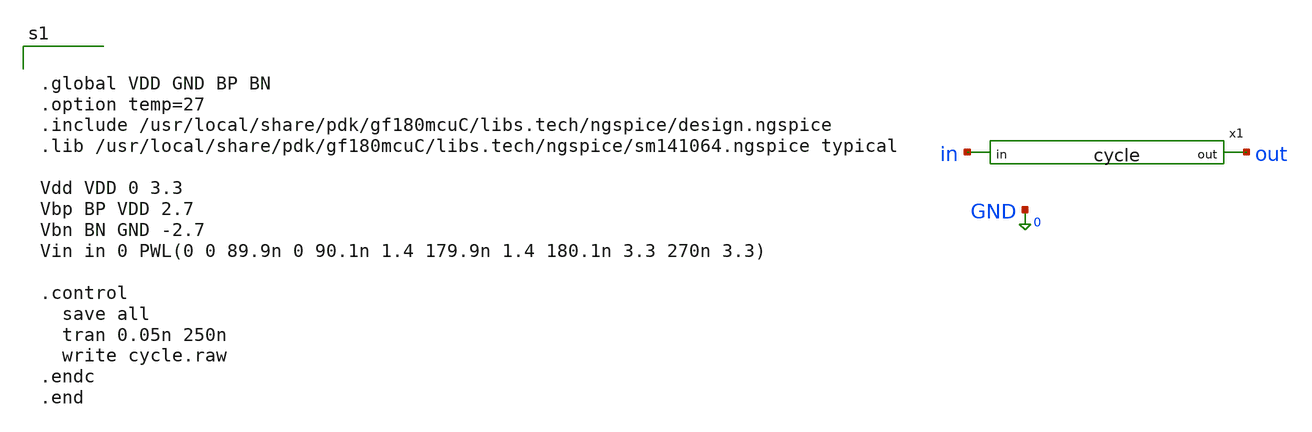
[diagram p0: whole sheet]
** sch_path: xschem_designs/cycle_TB.sch
**.subckt cycle_TB
x1 out in cycle
**** begin user architecture code


.global VDD GND BP BN
.option temp=27
.include /usr/local/share/pdk/gf180mcuC/libs.tech/ngspice/design.ngspice
.lib /usr/local/share/pdk/gf180mcuC/libs.tech/ngspice/sm141064.ngspice typical

Vdd VDD 0 3.3
Vbp BP VDD 2.7
Vbn BN GND -2.7
Vin in 0 PWL(0 0 89.9n 0 90.1n 1.4 179.9n 1.4 180.1n 3.3 270n 3.3)

.control
  save all
  tran 0.05n 250n
  write cycle.raw
.endc
.end


**** end user architecture code
**.ends

* expanding   symbol:  xschem_designs/cycle.sym # of pins=2
** sym_path: xschem_designs/cycle.sym
** sch_path: xschem_designs/cycle.sch
.subckt cycle out in
*.ipin in
*.opin out
XM225 out out net2 GND nfet_03v3 L=2.24u W=0.22u nf=1 ad='int((nf+1)/2) * W/nf * 0.18u' as='int((nf+2)/2) * W/nf * 0.18u'
+ pd='2*int((nf+1)/2) * (W/nf + 0.18u)' ps='2*int((nf+2)/2) * (W/nf + 0.18u)' nrd='0.18u / W' nrs='0.18u / W'
+ sa=0 sb=0 sd=0 m=1 par=1
XM226 out out net3 VDD pfet_03v3 L=1.12u W=0.22u nf=1 ad='int((nf+1)/2) * W/nf * 0.18u' as='int((nf+2)/2) * W/nf * 0.18u'
+ pd='2*int((nf+1)/2) * (W/nf + 0.18u)' ps='2*int((nf+2)/2) * (W/nf + 0.18u)' nrd='0.18u / W' nrs='0.18u / W'
+ sa=0 sb=0 sd=0 m=1 par=1
XM237 net3 in VDD VDD pfet_03v3 L=0.28u W=0.44u nf=1 ad='int((nf+1)/2) * W/nf * 0.18u' as='int((nf+2)/2) * W/nf * 0.18u'
+ pd='2*int((nf+1)/2) * (W/nf + 0.18u)' ps='2*int((nf+2)/2) * (W/nf + 0.18u)' nrd='0.18u / W' nrs='0.18u / W'
+ sa=0 sb=0 sd=0 m=1 par=1
XM238 net2 NTI GND GND nfet_03v3 L=0.28u W=0.22u nf=1 ad='int((nf+1)/2) * W/nf * 0.18u' as='int((nf+2)/2) * W/nf * 0.18u'
+ pd='2*int((nf+1)/2) * (W/nf + 0.18u)' ps='2*int((nf+2)/2) * (W/nf + 0.18u)' nrd='0.18u / W' nrs='0.18u / W'
+ sa=0 sb=0 sd=0 m=1 par=1
XM241 out net1 VDD BP pfet_06v0 L=1.1u W=0.60u nf=1 ad='int((nf+1)/2) * W/nf * 0.18u' as='int((nf+2)/2) * W/nf * 0.18u'
+ pd='2*int((nf+1)/2) * (W/nf + 0.18u)' ps='2*int((nf+2)/2) * (W/nf + 0.18u)' nrd='0.18u / W' nrs='0.18u / W'
+ sa=0 sb=0 sd=0 m=1 par=1
XM242 out in GND BN nfet_06v0 L=1.4u W=0.30u nf=1 ad='int((nf+1)/2) * W/nf * 0.18u' as='int((nf+2)/2) * W/nf * 0.18u'
+ pd='2*int((nf+1)/2) * (W/nf + 0.18u)' ps='2*int((nf+2)/2) * (W/nf + 0.18u)' nrd='0.18u / W' nrs='0.18u / W'
+ sa=0 sb=0 sd=0 m=1 par=1
XM1 NTI in GND GND nfet_03v3 L=0.28u W=0.22u nf=1 ad='int((nf+1)/2) * W/nf * 0.18u' as='int((nf+2)/2) * W/nf * 0.18u'
+ pd='2*int((nf+1)/2) * (W/nf + 0.18u)' ps='2*int((nf+2)/2) * (W/nf + 0.18u)' nrd='0.18u / W' nrs='0.18u / W'
+ sa=0 sb=0 sd=0 m=1 par=1
XM2 PTI in GND BN nfet_06v0 L=1.4u W=0.30u nf=1 ad='int((nf+1)/2) * W/nf * 0.18u' as='int((nf+2)/2) * W/nf * 0.18u'
+ pd='2*int((nf+1)/2) * (W/nf + 0.18u)' ps='2*int((nf+2)/2) * (W/nf + 0.18u)' nrd='0.18u / W' nrs='0.18u / W'
+ sa=0 sb=0 sd=0 m=1 par=1
XM3 NTI in VDD BP pfet_06v0 L=1.1u W=0.60u nf=1 ad='int((nf+1)/2) * W/nf * 0.18u' as='int((nf+2)/2) * W/nf * 0.18u'
+ pd='2*int((nf+1)/2) * (W/nf + 0.18u)' ps='2*int((nf+2)/2) * (W/nf + 0.18u)' nrd='0.18u / W' nrs='0.18u / W'
+ sa=0 sb=0 sd=0 m=1 par=1
XM4 PTI in VDD VDD pfet_03v3 L=0.28u W=0.44u nf=1 ad='int((nf+1)/2) * W/nf * 0.18u' as='int((nf+2)/2) * W/nf * 0.18u'
+ pd='2*int((nf+1)/2) * (W/nf + 0.18u)' ps='2*int((nf+2)/2) * (W/nf + 0.18u)' nrd='0.18u / W' nrs='0.18u / W'
+ sa=0 sb=0 sd=0 m=1 par=1
XM11 net4 in GND GND nfet_03v3 L=0.28u W=0.22u nf=1 ad='int((nf+1)/2) * W/nf * 0.18u' as='int((nf+2)/2) * W/nf * 0.18u'
+ pd='2*int((nf+1)/2) * (W/nf + 0.18u)' ps='2*int((nf+2)/2) * (W/nf + 0.18u)' nrd='0.18u / W' nrs='0.18u / W'
+ sa=0 sb=0 sd=0 m=1 par=1
XM12 net1 PTI net4 GND nfet_03v3 L=0.28u W=0.22u nf=1 ad='int((nf+1)/2) * W/nf * 0.18u' as='int((nf+2)/2) * W/nf * 0.18u'
+ pd='2*int((nf+1)/2) * (W/nf + 0.18u)' ps='2*int((nf+2)/2) * (W/nf + 0.18u)' nrd='0.18u / W' nrs='0.18u / W'
+ sa=0 sb=0 sd=0 m=1 par=1
XM13 net1 in VDD BP pfet_06v0 L=1.1u W=0.60u nf=1 ad='int((nf+1)/2) * W/nf * 0.18u' as='int((nf+2)/2) * W/nf * 0.18u'
+ pd='2*int((nf+1)/2) * (W/nf + 0.18u)' ps='2*int((nf+2)/2) * (W/nf + 0.18u)' nrd='0.18u / W' nrs='0.18u / W'
+ sa=0 sb=0 sd=0 m=1 par=1
XM14 net1 PTI VDD BP pfet_06v0 L=1.1u W=0.60u nf=1 ad='int((nf+1)/2) * W/nf * 0.18u' as='int((nf+2)/2) * W/nf * 0.18u'
+ pd='2*int((nf+1)/2) * (W/nf + 0.18u)' ps='2*int((nf+2)/2) * (W/nf + 0.18u)' nrd='0.18u / W' nrs='0.18u / W'
+ sa=0 sb=0 sd=0 m=1 par=1
.ends

.end
